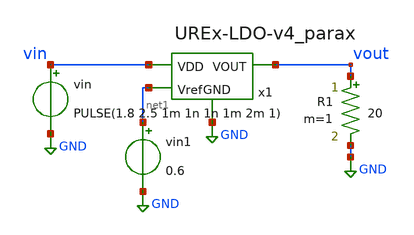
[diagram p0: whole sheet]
** sch_path: xschem/testbenches/postlayout/LineReg-v4-postlayout.sch
**.subckt LineReg-v4-postlayout
vin vin GND PULSE(1.8 2.5 1m 1n 1n 1m 2m 1)
R1 vout GND 20 m=1
x1 vin vout GND net1 UREx-LDO-v4_parax
vin1 net1 GND 0.6
**** begin user architecture code



.lib /usr/local/share/pdk/sky130A/libs.tech/ngspice/sky130.lib.spice tt
.tran 1u 3m

.control
run
plot v(vout)
.endc


**** end user architecture code
**.ends

* expanding   symbol:  UREx-LDO-v4_parax.sym # of pins=4
** sym_path: xschem/UREx-LDO-v4.sym
.include [file normalize UREx-LDO-v4_parax.spice]
.GLOBAL GND
.end
